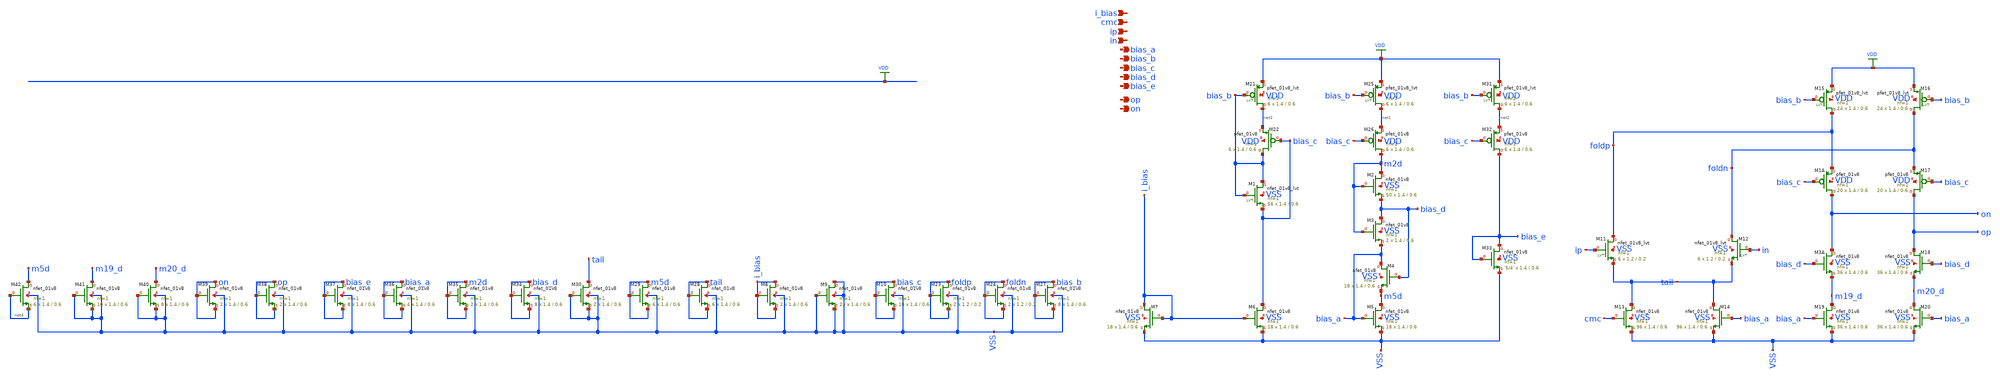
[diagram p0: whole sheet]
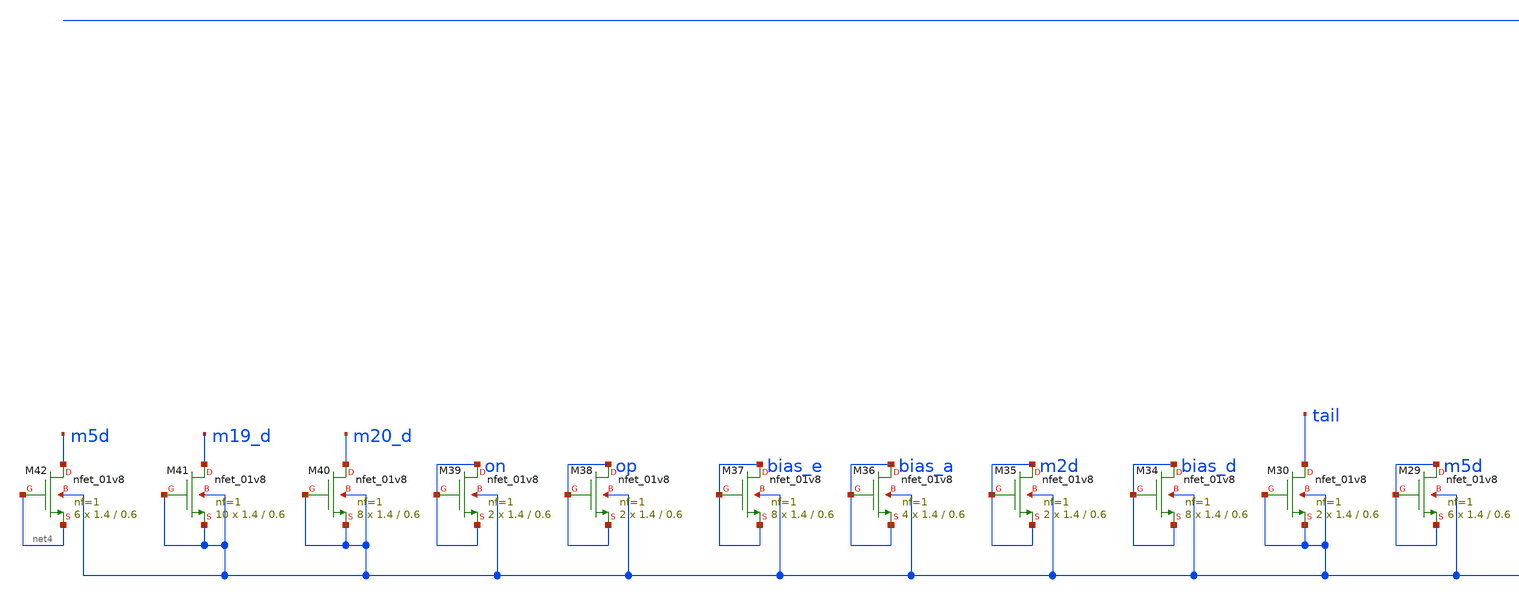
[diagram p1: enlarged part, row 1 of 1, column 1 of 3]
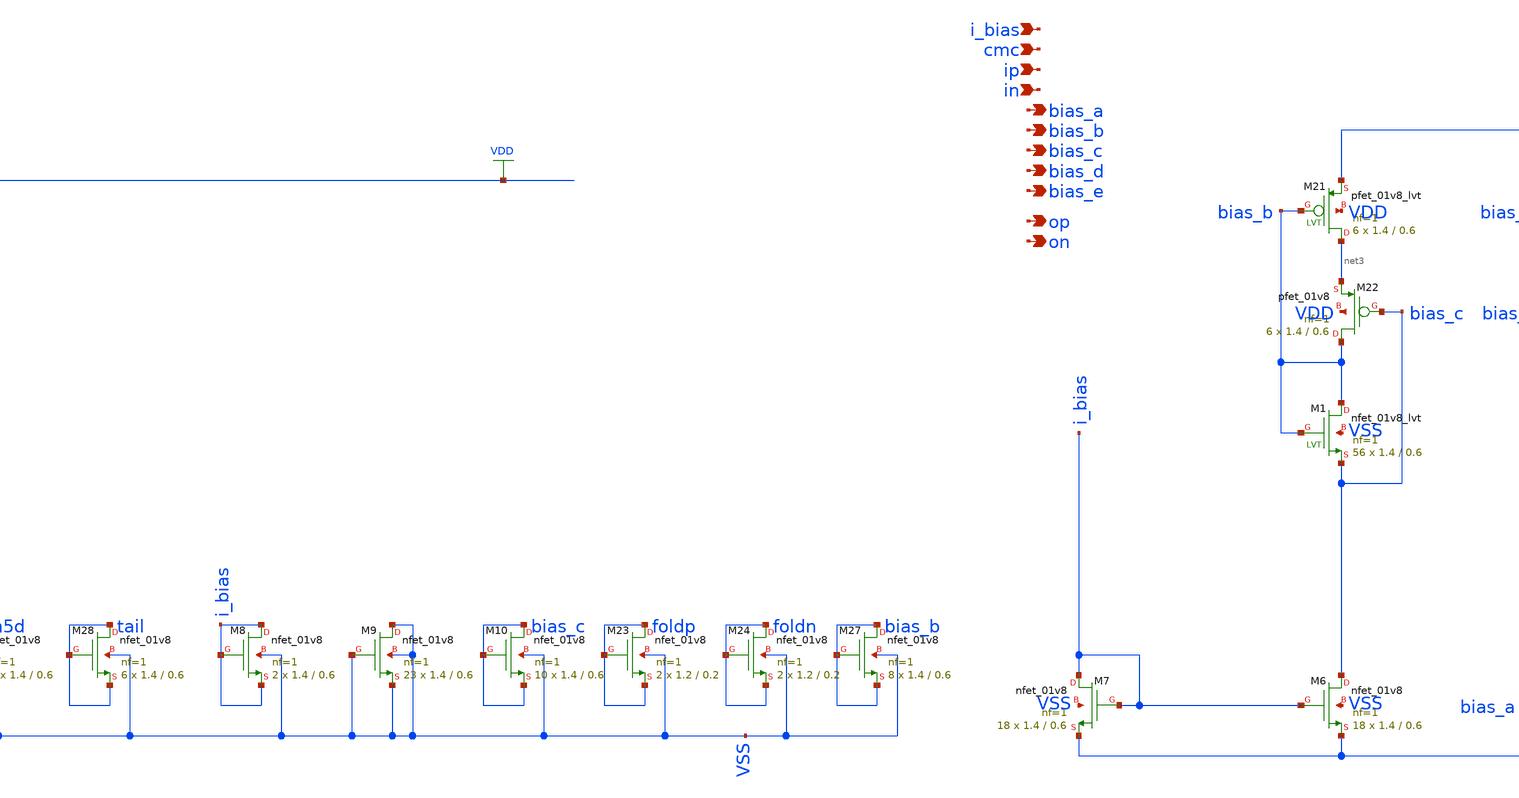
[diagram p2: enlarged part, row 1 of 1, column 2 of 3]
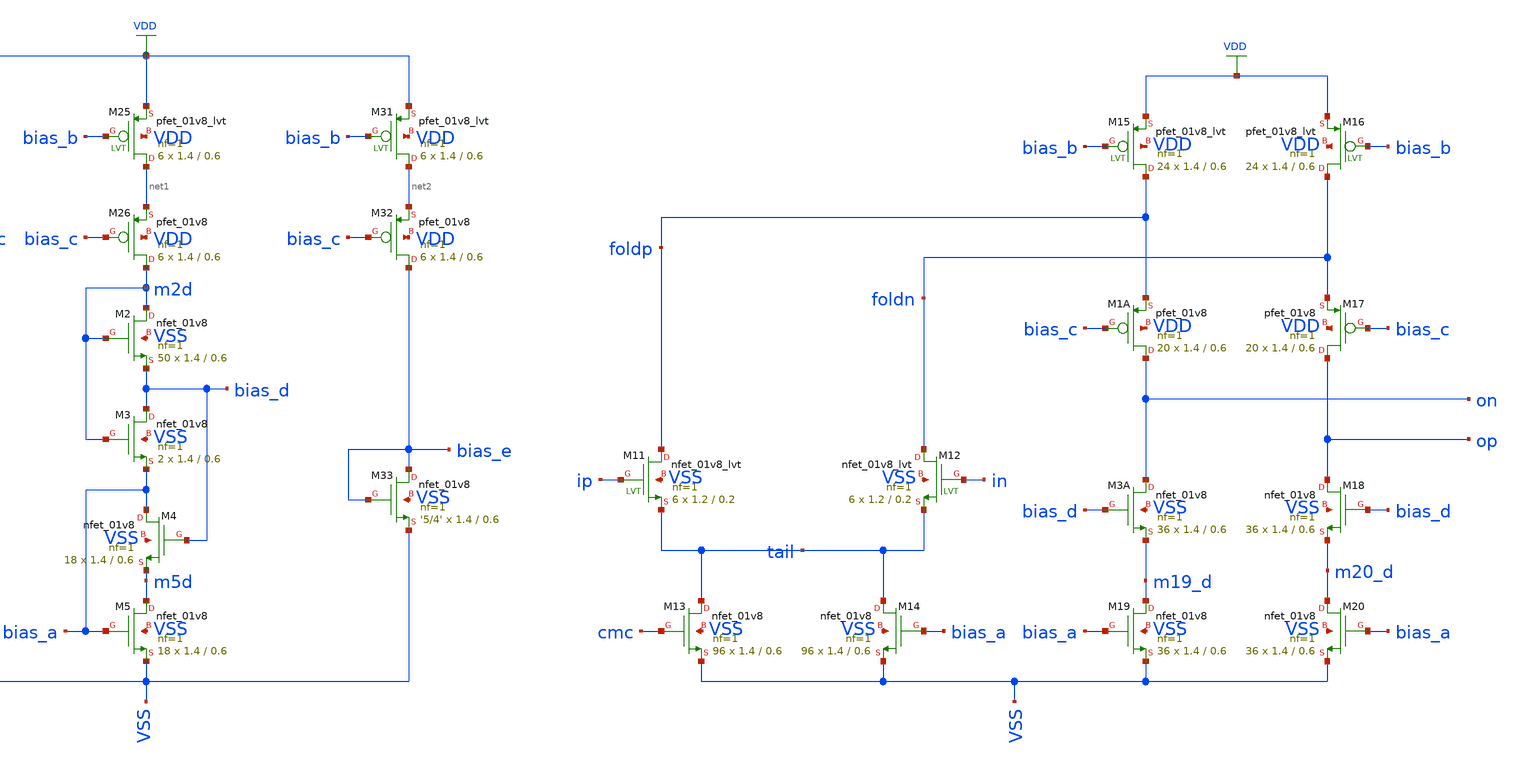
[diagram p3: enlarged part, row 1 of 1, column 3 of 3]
** sch_path: design/analog_modulator/schematic/ota_lvs.sch
**.subckt ota_lvs ip in op on i_bias bias_e bias_a bias_b bias_c bias_d cmc
*.ipin ip
*.ipin in
*.opin op
*.opin on
*.ipin i_bias
*.opin bias_e
*.opin bias_a
*.opin bias_b
*.opin bias_c
*.opin bias_d
*.ipin cmc
XM22 bias_b bias_c net3 VDD sky130_fd_pr__pfet_01v8 L=0.6 W=1.4 nf=1 ad='int((nf+1)/2) * W/nf * 0.29'
+ as='int((nf+2)/2) * W/nf * 0.29' pd='2*int((nf+1)/2) * (W/nf + 0.29)' ps='2*int((nf+2)/2) * (W/nf + 0.29)'
+ nrd='0.29 / W' nrs='0.29 / W' sa=0 sb=0 sd=0 mult=6 m=6
XM26 m2d bias_c net1 VDD sky130_fd_pr__pfet_01v8 L=0.6 W=1.4 nf=1 ad='int((nf+1)/2) * W/nf * 0.29' as='int((nf+2)/2) * W/nf * 0.29'
+ pd='2*int((nf+1)/2) * (W/nf + 0.29)' ps='2*int((nf+2)/2) * (W/nf + 0.29)' nrd='0.29 / W' nrs='0.29 / W'
+ sa=0 sb=0 sd=0 mult=6 m=6
XM32 bias_e bias_c net2 VDD sky130_fd_pr__pfet_01v8 L=0.6 W=1.4 nf=1 ad='int((nf+1)/2) * W/nf * 0.29'
+ as='int((nf+2)/2) * W/nf * 0.29' pd='2*int((nf+1)/2) * (W/nf + 0.29)' ps='2*int((nf+2)/2) * (W/nf + 0.29)'
+ nrd='0.29 / W' nrs='0.29 / W' sa=0 sb=0 sd=0 mult=6 m=6
XM33 bias_e bias_e VSS VSS sky130_fd_pr__nfet_01v8 L=0.6 W=1.4 nf=1 ad='int((nf+1)/2) * W/nf * 0.29'
+ as='int((nf+2)/2) * W/nf * 0.29' pd='2*int((nf+1)/2) * (W/nf + 0.29)' ps='2*int((nf+2)/2) * (W/nf + 0.29)'
+ nrd='0.29 / W' nrs='0.29 / W' sa=0 sb=0 sd=0 mult='5/4' m='5/4'
XM21 net3 bias_b VDD VDD sky130_fd_pr__pfet_01v8_lvt L=0.6 W=1.4 nf=1 ad='int((nf+1)/2) * W/nf * 0.29'
+ as='int((nf+2)/2) * W/nf * 0.29' pd='2*int((nf+1)/2) * (W/nf + 0.29)' ps='2*int((nf+2)/2) * (W/nf + 0.29)'
+ nrd='0.29 / W' nrs='0.29 / W' sa=0 sb=0 sd=0 mult=6 m=6
XM25 net1 bias_b VDD VDD sky130_fd_pr__pfet_01v8_lvt L=0.6 W=1.4 nf=1 ad='int((nf+1)/2) * W/nf * 0.29'
+ as='int((nf+2)/2) * W/nf * 0.29' pd='2*int((nf+1)/2) * (W/nf + 0.29)' ps='2*int((nf+2)/2) * (W/nf + 0.29)'
+ nrd='0.29 / W' nrs='0.29 / W' sa=0 sb=0 sd=0 mult=6 m=6
XM31 net2 bias_b VDD VDD sky130_fd_pr__pfet_01v8_lvt L=0.6 W=1.4 nf=1 ad='int((nf+1)/2) * W/nf * 0.29'
+ as='int((nf+2)/2) * W/nf * 0.29' pd='2*int((nf+1)/2) * (W/nf + 0.29)' ps='2*int((nf+2)/2) * (W/nf + 0.29)'
+ nrd='0.29 / W' nrs='0.29 / W' sa=0 sb=0 sd=0 mult=6 m=6
XM1 bias_b bias_b bias_c VSS sky130_fd_pr__nfet_01v8_lvt L=0.6 W=1.4 nf=1 ad='int((nf+1)/2) * W/nf * 0.29'
+ as='int((nf+2)/2) * W/nf * 0.29' pd='2*int((nf+1)/2) * (W/nf + 0.29)' ps='2*int((nf+2)/2) * (W/nf + 0.29)'
+ nrd='0.29 / W' nrs='0.29 / W' sa=0 sb=0 sd=0 mult=56 m=56
XM2 m2d m2d bias_d VSS sky130_fd_pr__nfet_01v8 L=0.6 W=1.4 nf=1 ad='int((nf+1)/2) * W/nf * 0.29' as='int((nf+2)/2) * W/nf * 0.29'
+ pd='2*int((nf+1)/2) * (W/nf + 0.29)' ps='2*int((nf+2)/2) * (W/nf + 0.29)' nrd='0.29 / W' nrs='0.29 / W'
+ sa=0 sb=0 sd=0 mult=50 m=50
XM3 bias_d m2d bias_a VSS sky130_fd_pr__nfet_01v8 L=0.6 W=1.4 nf=1 ad='int((nf+1)/2) * W/nf * 0.29' as='int((nf+2)/2) * W/nf * 0.29'
+ pd='2*int((nf+1)/2) * (W/nf + 0.29)' ps='2*int((nf+2)/2) * (W/nf + 0.29)' nrd='0.29 / W' nrs='0.29 / W'
+ sa=0 sb=0 sd=0 mult=2 m=2
XM4 bias_a bias_d m5d VSS sky130_fd_pr__nfet_01v8 L=0.6 W=1.4 nf=1 ad='int((nf+1)/2) * W/nf * 0.29' as='int((nf+2)/2) * W/nf * 0.29'
+ pd='2*int((nf+1)/2) * (W/nf + 0.29)' ps='2*int((nf+2)/2) * (W/nf + 0.29)' nrd='0.29 / W' nrs='0.29 / W'
+ sa=0 sb=0 sd=0 mult=18 m=18
XM5 m5d bias_a VSS VSS sky130_fd_pr__nfet_01v8 L=0.6 W=1.4 nf=1 ad='int((nf+1)/2) * W/nf * 0.29' as='int((nf+2)/2) * W/nf * 0.29'
+ pd='2*int((nf+1)/2) * (W/nf + 0.29)' ps='2*int((nf+2)/2) * (W/nf + 0.29)' nrd='0.29 / W' nrs='0.29 / W'
+ sa=0 sb=0 sd=0 mult=18 m=18
XM6 bias_c i_bias VSS VSS sky130_fd_pr__nfet_01v8 L=0.6 W=1.4 nf=1 ad='int((nf+1)/2) * W/nf * 0.29' as='int((nf+2)/2) * W/nf * 0.29'
+ pd='2*int((nf+1)/2) * (W/nf + 0.29)' ps='2*int((nf+2)/2) * (W/nf + 0.29)' nrd='0.29 / W' nrs='0.29 / W'
+ sa=0 sb=0 sd=0 mult=18 m=18
XM7 i_bias i_bias VSS VSS sky130_fd_pr__nfet_01v8 L=0.6 W=1.4 nf=1 ad='int((nf+1)/2) * W/nf * 0.29' as='int((nf+2)/2) * W/nf * 0.29'
+ pd='2*int((nf+1)/2) * (W/nf + 0.29)' ps='2*int((nf+2)/2) * (W/nf + 0.29)' nrd='0.29 / W' nrs='0.29 / W'
+ sa=0 sb=0 sd=0 mult=18 m=18
XM8 i_bias i_bias i_bias VSS sky130_fd_pr__nfet_01v8 L=0.6 W=1.4 nf=1 ad='int((nf+1)/2) * W/nf * 0.29'
+ as='int((nf+2)/2) * W/nf * 0.29' pd='2*int((nf+1)/2) * (W/nf + 0.29)' ps='2*int((nf+2)/2) * (W/nf + 0.29)'
+ nrd='0.29 / W' nrs='0.29 / W' sa=0 sb=0 sd=0 mult=2 m=2
XM9 VSS VSS VSS VSS sky130_fd_pr__nfet_01v8 L=0.6 W=1.4 nf=1 ad='int((nf+1)/2) * W/nf * 0.29' as='int((nf+2)/2) * W/nf * 0.29'
+ pd='2*int((nf+1)/2) * (W/nf + 0.29)' ps='2*int((nf+2)/2) * (W/nf + 0.29)' nrd='0.29 / W' nrs='0.29 / W'
+ sa=0 sb=0 sd=0 mult=23 m=23
XM10 bias_c bias_c bias_c VSS sky130_fd_pr__nfet_01v8 L=0.6 W=1.4 nf=1 ad='int((nf+1)/2) * W/nf * 0.29'
+ as='int((nf+2)/2) * W/nf * 0.29' pd='2*int((nf+1)/2) * (W/nf + 0.29)' ps='2*int((nf+2)/2) * (W/nf + 0.29)'
+ nrd='0.29 / W' nrs='0.29 / W' sa=0 sb=0 sd=0 mult=10 m=10
XM11 foldp ip tail VSS sky130_fd_pr__nfet_01v8_lvt L=0.2 W=1.2 nf=1 ad='int((nf+1)/2) * W/nf * 0.29'
+ as='int((nf+2)/2) * W/nf * 0.29' pd='2*int((nf+1)/2) * (W/nf + 0.29)' ps='2*int((nf+2)/2) * (W/nf + 0.29)'
+ nrd='0.29 / W' nrs='0.29 / W' sa=0 sb=0 sd=0 mult=6 m=6
XM12 foldn in tail VSS sky130_fd_pr__nfet_01v8_lvt L=0.2 W=1.2 nf=1 ad='int((nf+1)/2) * W/nf * 0.29'
+ as='int((nf+2)/2) * W/nf * 0.29' pd='2*int((nf+1)/2) * (W/nf + 0.29)' ps='2*int((nf+2)/2) * (W/nf + 0.29)'
+ nrd='0.29 / W' nrs='0.29 / W' sa=0 sb=0 sd=0 mult=6 m=6
XM13 tail cmc VSS VSS sky130_fd_pr__nfet_01v8 L=0.6 W=1.4 nf=1 ad='int((nf+1)/2) * W/nf * 0.29' as='int((nf+2)/2) * W/nf * 0.29'
+ pd='2*int((nf+1)/2) * (W/nf + 0.29)' ps='2*int((nf+2)/2) * (W/nf + 0.29)' nrd='0.29 / W' nrs='0.29 / W'
+ sa=0 sb=0 sd=0 mult=96 m=96
XM14 tail bias_a VSS VSS sky130_fd_pr__nfet_01v8 L=0.6 W=1.4 nf=1 ad='int((nf+1)/2) * W/nf * 0.29' as='int((nf+2)/2) * W/nf * 0.29'
+ pd='2*int((nf+1)/2) * (W/nf + 0.29)' ps='2*int((nf+2)/2) * (W/nf + 0.29)' nrd='0.29 / W' nrs='0.29 / W'
+ sa=0 sb=0 sd=0 mult=96 m=96
XM15 foldp bias_b VDD VDD sky130_fd_pr__pfet_01v8_lvt L=0.6 W=1.4 nf=1 ad='int((nf+1)/2) * W/nf * 0.29'
+ as='int((nf+2)/2) * W/nf * 0.29' pd='2*int((nf+1)/2) * (W/nf + 0.29)' ps='2*int((nf+2)/2) * (W/nf + 0.29)'
+ nrd='0.29 / W' nrs='0.29 / W' sa=0 sb=0 sd=0 mult=24 m=24
XM16 foldn bias_b VDD VDD sky130_fd_pr__pfet_01v8_lvt L=0.6 W=1.4 nf=1 ad='int((nf+1)/2) * W/nf * 0.29'
+ as='int((nf+2)/2) * W/nf * 0.29' pd='2*int((nf+1)/2) * (W/nf + 0.29)' ps='2*int((nf+2)/2) * (W/nf + 0.29)'
+ nrd='0.29 / W' nrs='0.29 / W' sa=0 sb=0 sd=0 mult=24 m=24
XM1A on bias_c foldp VDD sky130_fd_pr__pfet_01v8 L=0.6 W=1.4 nf=1 ad='int((nf+1)/2) * W/nf * 0.29' as='int((nf+2)/2) * W/nf * 0.29'
+ pd='2*int((nf+1)/2) * (W/nf + 0.29)' ps='2*int((nf+2)/2) * (W/nf + 0.29)' nrd='0.29 / W' nrs='0.29 / W'
+ sa=0 sb=0 sd=0 mult=20 m=20
XM17 op bias_c foldn VDD sky130_fd_pr__pfet_01v8 L=0.6 W=1.4 nf=1 ad='int((nf+1)/2) * W/nf * 0.29' as='int((nf+2)/2) * W/nf * 0.29'
+ pd='2*int((nf+1)/2) * (W/nf + 0.29)' ps='2*int((nf+2)/2) * (W/nf + 0.29)' nrd='0.29 / W' nrs='0.29 / W'
+ sa=0 sb=0 sd=0 mult=20 m=20
XM3A on bias_d m19_d VSS sky130_fd_pr__nfet_01v8 L=0.6 W=1.4 nf=1 ad='int((nf+1)/2) * W/nf * 0.29' as='int((nf+2)/2) * W/nf * 0.29'
+ pd='2*int((nf+1)/2) * (W/nf + 0.29)' ps='2*int((nf+2)/2) * (W/nf + 0.29)' nrd='0.29 / W' nrs='0.29 / W'
+ sa=0 sb=0 sd=0 mult=36 m=36
XM18 op bias_d m20_d VSS sky130_fd_pr__nfet_01v8 L=0.6 W=1.4 nf=1 ad='int((nf+1)/2) * W/nf * 0.29' as='int((nf+2)/2) * W/nf * 0.29'
+ pd='2*int((nf+1)/2) * (W/nf + 0.29)' ps='2*int((nf+2)/2) * (W/nf + 0.29)' nrd='0.29 / W' nrs='0.29 / W'
+ sa=0 sb=0 sd=0 mult=36 m=36
XM19 m19_d bias_a VSS VSS sky130_fd_pr__nfet_01v8 L=0.6 W=1.4 nf=1 ad='int((nf+1)/2) * W/nf * 0.29' as='int((nf+2)/2) * W/nf * 0.29'
+ pd='2*int((nf+1)/2) * (W/nf + 0.29)' ps='2*int((nf+2)/2) * (W/nf + 0.29)' nrd='0.29 / W' nrs='0.29 / W'
+ sa=0 sb=0 sd=0 mult=36 m=36
XM20 m20_d bias_a VSS VSS sky130_fd_pr__nfet_01v8 L=0.6 W=1.4 nf=1 ad='int((nf+1)/2) * W/nf * 0.29' as='int((nf+2)/2) * W/nf * 0.29'
+ pd='2*int((nf+1)/2) * (W/nf + 0.29)' ps='2*int((nf+2)/2) * (W/nf + 0.29)' nrd='0.29 / W' nrs='0.29 / W'
+ sa=0 sb=0 sd=0 mult=36 m=36
XM23 foldp foldp foldp VSS sky130_fd_pr__nfet_01v8 L=0.2 W=1.2 nf=1 ad='int((nf+1)/2) * W/nf * 0.29'
+ as='int((nf+2)/2) * W/nf * 0.29' pd='2*int((nf+1)/2) * (W/nf + 0.29)' ps='2*int((nf+2)/2) * (W/nf + 0.29)'
+ nrd='0.29 / W' nrs='0.29 / W' sa=0 sb=0 sd=0 mult=2 m=2
XM24 foldn foldn foldn VSS sky130_fd_pr__nfet_01v8 L=0.2 W=1.2 nf=1 ad='int((nf+1)/2) * W/nf * 0.29'
+ as='int((nf+2)/2) * W/nf * 0.29' pd='2*int((nf+1)/2) * (W/nf + 0.29)' ps='2*int((nf+2)/2) * (W/nf + 0.29)'
+ nrd='0.29 / W' nrs='0.29 / W' sa=0 sb=0 sd=0 mult=2 m=2
XM27 bias_b bias_b bias_b VSS sky130_fd_pr__nfet_01v8 L=0.6 W=1.4 nf=1 ad='int((nf+1)/2) * W/nf * 0.29'
+ as='int((nf+2)/2) * W/nf * 0.29' pd='2*int((nf+1)/2) * (W/nf + 0.29)' ps='2*int((nf+2)/2) * (W/nf + 0.29)'
+ nrd='0.29 / W' nrs='0.29 / W' sa=0 sb=0 sd=0 mult=8 m=8
XM28 tail tail tail VSS sky130_fd_pr__nfet_01v8 L=0.6 W=1.4 nf=1 ad='int((nf+1)/2) * W/nf * 0.29' as='int((nf+2)/2) * W/nf * 0.29'
+ pd='2*int((nf+1)/2) * (W/nf + 0.29)' ps='2*int((nf+2)/2) * (W/nf + 0.29)' nrd='0.29 / W' nrs='0.29 / W'
+ sa=0 sb=0 sd=0 mult=6 m=6
XM29 m5d m5d m5d VSS sky130_fd_pr__nfet_01v8 L=0.6 W=1.4 nf=1 ad='int((nf+1)/2) * W/nf * 0.29' as='int((nf+2)/2) * W/nf * 0.29'
+ pd='2*int((nf+1)/2) * (W/nf + 0.29)' ps='2*int((nf+2)/2) * (W/nf + 0.29)' nrd='0.29 / W' nrs='0.29 / W'
+ sa=0 sb=0 sd=0 mult=6 m=6
XM30 tail VSS VSS VSS sky130_fd_pr__nfet_01v8 L=0.6 W=1.4 nf=1 ad='int((nf+1)/2) * W/nf * 0.29' as='int((nf+2)/2) * W/nf * 0.29'
+ pd='2*int((nf+1)/2) * (W/nf + 0.29)' ps='2*int((nf+2)/2) * (W/nf + 0.29)' nrd='0.29 / W' nrs='0.29 / W'
+ sa=0 sb=0 sd=0 mult=2 m=2
XM34 bias_d bias_d bias_d VSS sky130_fd_pr__nfet_01v8 L=0.6 W=1.4 nf=1 ad='int((nf+1)/2) * W/nf * 0.29'
+ as='int((nf+2)/2) * W/nf * 0.29' pd='2*int((nf+1)/2) * (W/nf + 0.29)' ps='2*int((nf+2)/2) * (W/nf + 0.29)'
+ nrd='0.29 / W' nrs='0.29 / W' sa=0 sb=0 sd=0 mult=8 m=8
XM35 m2d m2d m2d VSS sky130_fd_pr__nfet_01v8 L=0.6 W=1.4 nf=1 ad='int((nf+1)/2) * W/nf * 0.29' as='int((nf+2)/2) * W/nf * 0.29'
+ pd='2*int((nf+1)/2) * (W/nf + 0.29)' ps='2*int((nf+2)/2) * (W/nf + 0.29)' nrd='0.29 / W' nrs='0.29 / W'
+ sa=0 sb=0 sd=0 mult=2 m=2
XM36 bias_a bias_a bias_a VSS sky130_fd_pr__nfet_01v8 L=0.6 W=1.4 nf=1 ad='int((nf+1)/2) * W/nf * 0.29'
+ as='int((nf+2)/2) * W/nf * 0.29' pd='2*int((nf+1)/2) * (W/nf + 0.29)' ps='2*int((nf+2)/2) * (W/nf + 0.29)'
+ nrd='0.29 / W' nrs='0.29 / W' sa=0 sb=0 sd=0 mult=4 m=4
XM37 bias_e bias_e bias_e VSS sky130_fd_pr__nfet_01v8 L=0.6 W=1.4 nf=1 ad='int((nf+1)/2) * W/nf * 0.29'
+ as='int((nf+2)/2) * W/nf * 0.29' pd='2*int((nf+1)/2) * (W/nf + 0.29)' ps='2*int((nf+2)/2) * (W/nf + 0.29)'
+ nrd='0.29 / W' nrs='0.29 / W' sa=0 sb=0 sd=0 mult=8 m=8
XM38 op op op VSS sky130_fd_pr__nfet_01v8 L=0.6 W=1.4 nf=1 ad='int((nf+1)/2) * W/nf * 0.29' as='int((nf+2)/2) * W/nf * 0.29'
+ pd='2*int((nf+1)/2) * (W/nf + 0.29)' ps='2*int((nf+2)/2) * (W/nf + 0.29)' nrd='0.29 / W' nrs='0.29 / W'
+ sa=0 sb=0 sd=0 mult=2 m=2
XM39 on on on VSS sky130_fd_pr__nfet_01v8 L=0.6 W=1.4 nf=1 ad='int((nf+1)/2) * W/nf * 0.29' as='int((nf+2)/2) * W/nf * 0.29'
+ pd='2*int((nf+1)/2) * (W/nf + 0.29)' ps='2*int((nf+2)/2) * (W/nf + 0.29)' nrd='0.29 / W' nrs='0.29 / W'
+ sa=0 sb=0 sd=0 mult=2 m=2
XM40 m20_d VSS VSS VSS sky130_fd_pr__nfet_01v8 L=0.6 W=1.4 nf=1 ad='int((nf+1)/2) * W/nf * 0.29' as='int((nf+2)/2) * W/nf * 0.29'
+ pd='2*int((nf+1)/2) * (W/nf + 0.29)' ps='2*int((nf+2)/2) * (W/nf + 0.29)' nrd='0.29 / W' nrs='0.29 / W'
+ sa=0 sb=0 sd=0 mult=8 m=8
XM41 m19_d VSS VSS VSS sky130_fd_pr__nfet_01v8 L=0.6 W=1.4 nf=1 ad='int((nf+1)/2) * W/nf * 0.29' as='int((nf+2)/2) * W/nf * 0.29'
+ pd='2*int((nf+1)/2) * (W/nf + 0.29)' ps='2*int((nf+2)/2) * (W/nf + 0.29)' nrd='0.29 / W' nrs='0.29 / W'
+ sa=0 sb=0 sd=0 mult=10 m=10
XM42 m5d net4 net4 VSS sky130_fd_pr__nfet_01v8 L=0.6 W=1.4 nf=1 ad='int((nf+1)/2) * W/nf * 0.29' as='int((nf+2)/2) * W/nf * 0.29'
+ pd='2*int((nf+1)/2) * (W/nf + 0.29)' ps='2*int((nf+2)/2) * (W/nf + 0.29)' nrd='0.29 / W' nrs='0.29 / W'
+ sa=0 sb=0 sd=0 mult=6 m=6
**.ends
.GLOBAL VDD
.end
